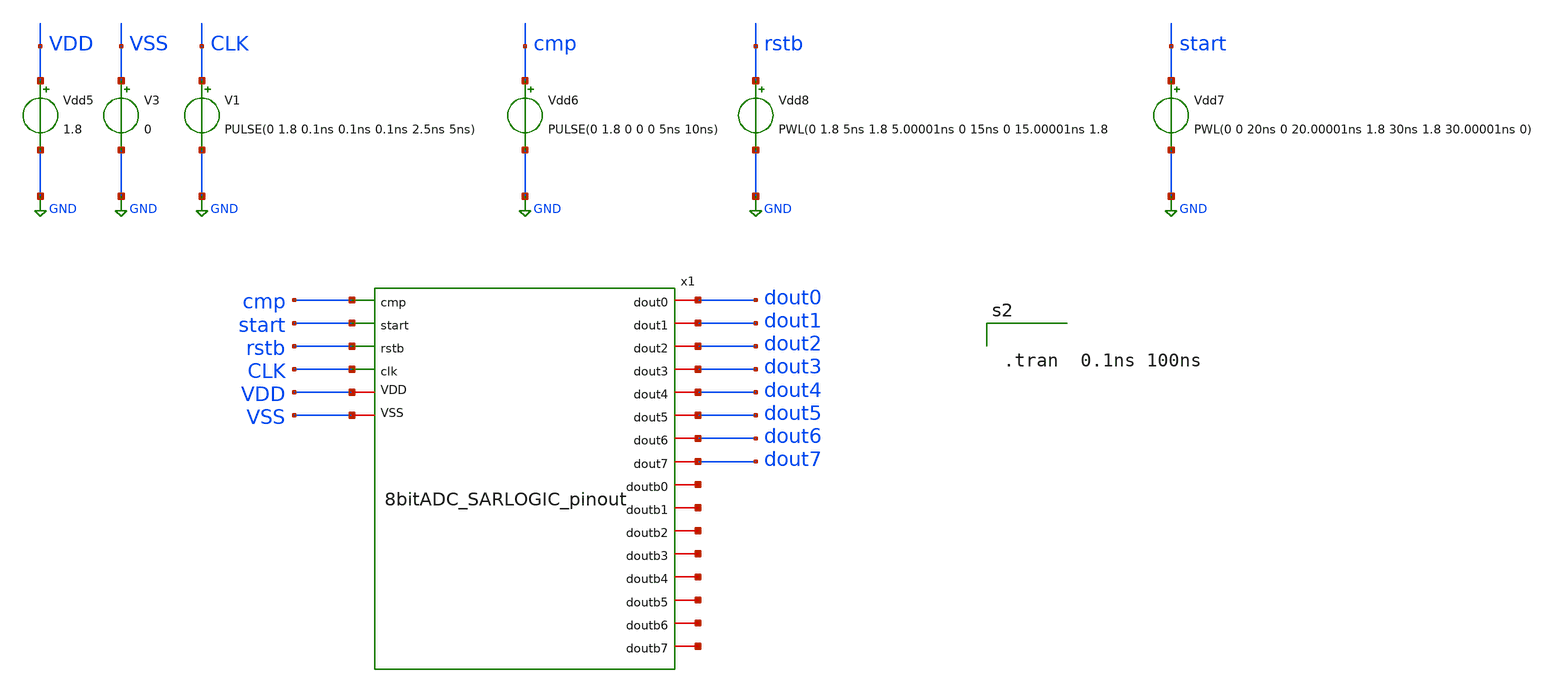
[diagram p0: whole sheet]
** sch_path: 8bitADC_SARLOGIC_tb.sch
**.subckt 8bitADC_SARLOGIC_tb
Vdd5 VDD GND 1.8
Vdd6 cmp GND PULSE(0 1.8 0 0 0 5ns 10ns)
V1 CLK GND PULSE(0 1.8 0.1ns 0.1ns 0.1ns 2.5ns 5ns)
V3 VSS GND 0
Vdd7 start GND PWL(0 0 20ns 0 20.00001ns 1.8 30ns 1.8 30.00001ns 0)
Vdd8 rstb GND PWL(0 1.8 5ns 1.8 5.00001ns 0 15ns 0 15.00001ns 1.8
x1 VDD cmp VSS start net1 dout0 rstb CLK net2 dout1 net3 dout2 dout3 net4 dout4 net5 dout5 net6
+ dout6 net7 net8 dout7 8bitADC_SARLOGIC_pinout
**** begin user architecture code

** opencircuitdesign pdks install
.lib $::SKYWATER_MODELS/sky130.lib.spice tt
.include $::SKYWATER_STDCELLS/sky130_fd_sc_hd.spice




.tran  0.1ns 100ns



**** end user architecture code
**.ends

* expanding   symbol:  8bitADC_SARLOGIC_pinout.sym # of pins=22
** sym_path: 8bitADC_SARLOGIC_pinout.sym
** sch_path: 8bitADC_SARLOGIC_pinout.sch
.subckt 8bitADC_SARLOGIC_pinout VDD cmp VSS start doutb0 dout0 rstb clk doutb1 dout1 doutb2 dout2
+ dout3 doutb3 dout4 doutb4 dout5 doutb5 dout6 doutb6 doutb7 dout7
*.ipin cmp
*.ipin start
*.ipin rstb
*.ipin clk
*.iopin dout0
*.iopin doutb0
*.iopin VSS
*.iopin VDD
*.iopin dout1
*.iopin dout2
*.iopin dout3
*.iopin dout4
*.iopin dout5
*.iopin dout6
*.iopin dout7
*.iopin doutb1
*.iopin doutb2
*.iopin doutb3
*.iopin doutb4
*.iopin doutb5
*.iopin doutb6
*.iopin doutb7
x19 clk VSS VNB VPB VDD clk_t sky130_fd_sc_hd__buf_1
x23 cmp VSS VNB VPB VDD net3 sky130_fd_sc_hd__buf_1
x24 net1 VSS VNB VPB VDD net2 sky130_fd_sc_hd__buf_1
x25 rstb VSS VNB VPB VDD net1 sky130_fd_sc_hd__buf_1
x26 start VSS VNB VPB VDD net11 sky130_fd_sc_hd__buf_1
x27 dout6 net3 net2 q1 VSS VNB VPB VDD dout7 doutb7 sky130_fd_sc_hd__dfbbn_2
x28 dout5 net3 net2 net5 VSS VNB VPB VDD dout6 doutb6 sky130_fd_sc_hd__dfbbn_2
x29 dout4 net3 net2 net6 VSS VNB VPB VDD dout5 doutb5 sky130_fd_sc_hd__dfbbn_2
x30 dout3 net3 net2 net7 VSS VNB VPB VDD dout4 doutb4 sky130_fd_sc_hd__dfbbn_2
x31 dout2 net3 net2 net4 VSS VNB VPB VDD dout3 doutb3 sky130_fd_sc_hd__dfbbn_2
x32 dout1 net3 net2 net8 VSS VNB VPB VDD dout2 doutb2 sky130_fd_sc_hd__dfbbn_2
x33 dout0 net3 net2 net9 VSS VNB VPB VDD dout1 doutb1 sky130_fd_sc_hd__dfbbn_2
x34 net19 net3 net2 net10 VSS VNB VPB VDD dout0 doutb0 sky130_fd_sc_hd__dfbbn_2
x35 clk_t net11 net2 VSS VNB VPB VDD q q1 sky130_fd_sc_hd__dfrbp_1
x36 clk_t q net2 VSS VNB VPB VDD net12 net5 sky130_fd_sc_hd__dfrbp_1
x37 clk_t net12 net2 VSS VNB VPB VDD net13 net6 sky130_fd_sc_hd__dfrbp_1
x38 clk_t net13 net2 VSS VNB VPB VDD net14 net7 sky130_fd_sc_hd__dfrbp_1
x39 clk_t net14 net2 VSS VNB VPB VDD net15 net4 sky130_fd_sc_hd__dfrbp_1
x40 clk_t net15 net2 VSS VNB VPB VDD net16 net8 sky130_fd_sc_hd__dfrbp_1
x41 clk_t net16 net2 VSS VNB VPB VDD net17 net9 sky130_fd_sc_hd__dfrbp_1
x42 clk_t net17 net2 VSS VNB VPB VDD net18 net10 sky130_fd_sc_hd__dfrbp_1
x43 clk_t net18 net2 VSS VNB VPB VDD net19 net20 sky130_fd_sc_hd__dfrbp_1
.ends

.GLOBAL GND
.end
